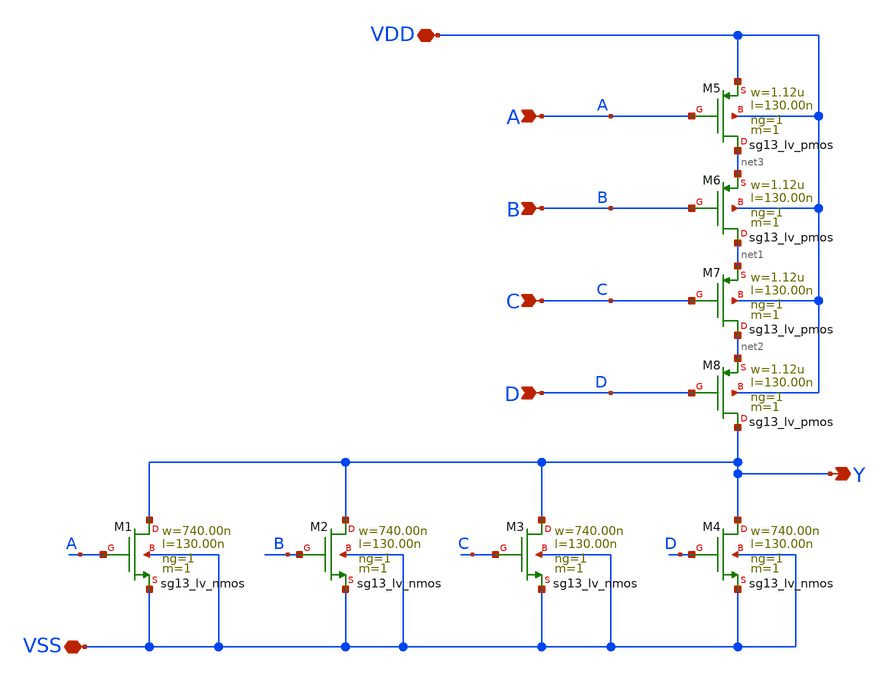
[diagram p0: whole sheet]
** sch_path: ihp-sg13g2/libs.tech/xschem/sg13g2_stdcells/sg13g2_nor4_1.sch
**.subckt sg13g2_nor4_1 Y A B C D VDD VSS
*.opin Y
*.ipin A
*.ipin B
*.ipin C
*.ipin D
*.iopin VDD
*.iopin VSS
XM1 Y A VSS VSS sg13_lv_nmos w=740.00n l=130.00n ng=1 m=1 mm_ok=1
XM2 Y B VSS VSS sg13_lv_nmos w=740.00n l=130.00n ng=1 m=1 mm_ok=1
XM3 Y C VSS VSS sg13_lv_nmos w=740.00n l=130.00n ng=1 m=1 mm_ok=1
XM4 Y D VSS VSS sg13_lv_nmos w=740.00n l=130.00n ng=1 m=1 mm_ok=1
XM5 net3 A VDD VDD sg13_lv_pmos w=1.12u l=130.00n ng=1 m=1 mm_ok=1
XM6 net1 B net3 VDD sg13_lv_pmos w=1.12u l=130.00n ng=1 m=1 mm_ok=1
XM7 net2 C net1 VDD sg13_lv_pmos w=1.12u l=130.00n ng=1 m=1 mm_ok=1
XM8 Y D net2 VDD sg13_lv_pmos w=1.12u l=130.00n ng=1 m=1 mm_ok=1
**.ends
.end
